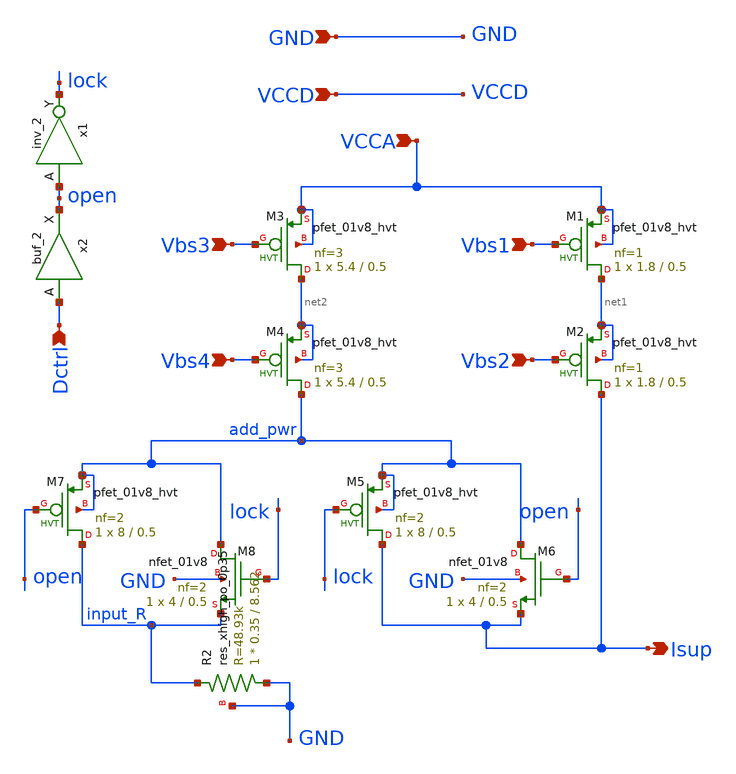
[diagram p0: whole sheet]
** sch_path: xschem/lib_dco/dco_idac.sch
**.subckt dco_idac Vbs3 Vbs4 Vbs1 Vbs2 Isup Dctrl VCCA GND VCCD
*.ipin Vbs3
*.ipin Vbs4
*.ipin Vbs1
*.ipin Vbs2
*.opin Isup
*.ipin Dctrl
*.ipin VCCA
*.ipin GND
*.ipin VCCD
x1 open GND GND VCCD VCCD lock sky130_fd_sc_hd__inv_2
XM1 net1 Vbs1 VCCA VCCA sky130_fd_pr__pfet_01v8_hvt L=0.5 W=1.8 nf=1 ad='int((nf+1)/2) * W/nf * 0.29'
+ as='int((nf+2)/2) * W/nf * 0.29' pd='2*int((nf+1)/2) * (W/nf + 0.29)' ps='2*int((nf+2)/2) * (W/nf + 0.29)'
+ nrd='0.29 / W' nrs='0.29 / W' sa=0 sb=0 sd=0 mult=1 m=1
XM2 Isup Vbs2 net1 net1 sky130_fd_pr__pfet_01v8_hvt L=0.5 W=1.8 nf=1 ad='int((nf+1)/2) * W/nf * 0.29'
+ as='int((nf+2)/2) * W/nf * 0.29' pd='2*int((nf+1)/2) * (W/nf + 0.29)' ps='2*int((nf+2)/2) * (W/nf + 0.29)'
+ nrd='0.29 / W' nrs='0.29 / W' sa=0 sb=0 sd=0 mult=1 m=1
x2 Dctrl GND GND VCCD VCCD open sky130_fd_sc_hd__buf_2
XM3 net2 Vbs3 VCCA VCCA sky130_fd_pr__pfet_01v8_hvt L=0.5 W=5.4 nf=3 ad='int((nf+1)/2) * W/nf * 0.29'
+ as='int((nf+2)/2) * W/nf * 0.29' pd='2*int((nf+1)/2) * (W/nf + 0.29)' ps='2*int((nf+2)/2) * (W/nf + 0.29)'
+ nrd='0.29 / W' nrs='0.29 / W' sa=0 sb=0 sd=0 mult=1 m=1
XM4 add_pwr Vbs4 net2 net2 sky130_fd_pr__pfet_01v8_hvt L=0.5 W=5.4 nf=3 ad='int((nf+1)/2) * W/nf * 0.29'
+ as='int((nf+2)/2) * W/nf * 0.29' pd='2*int((nf+1)/2) * (W/nf + 0.29)' ps='2*int((nf+2)/2) * (W/nf + 0.29)'
+ nrd='0.29 / W' nrs='0.29 / W' sa=0 sb=0 sd=0 mult=1 m=1
XM5 Isup lock add_pwr add_pwr sky130_fd_pr__pfet_01v8_hvt L=0.5 W=8 nf=2 ad='int((nf+1)/2) * W/nf * 0.29'
+ as='int((nf+2)/2) * W/nf * 0.29' pd='2*int((nf+1)/2) * (W/nf + 0.29)' ps='2*int((nf+2)/2) * (W/nf + 0.29)'
+ nrd='0.29 / W' nrs='0.29 / W' sa=0 sb=0 sd=0 mult=1 m=1
XM6 add_pwr open Isup GND sky130_fd_pr__nfet_01v8 L=0.5 W=4 nf=2 ad='int((nf+1)/2) * W/nf * 0.29' as='int((nf+2)/2) * W/nf * 0.29'
+ pd='2*int((nf+1)/2) * (W/nf + 0.29)' ps='2*int((nf+2)/2) * (W/nf + 0.29)' nrd='0.29 / W' nrs='0.29 / W'
+ sa=0 sb=0 sd=0 mult=1 m=1
XM7 input_R open add_pwr add_pwr sky130_fd_pr__pfet_01v8_hvt L=0.5 W=8 nf=2 ad='int((nf+1)/2) * W/nf * 0.29'
+ as='int((nf+2)/2) * W/nf * 0.29' pd='2*int((nf+1)/2) * (W/nf + 0.29)' ps='2*int((nf+2)/2) * (W/nf + 0.29)'
+ nrd='0.29 / W' nrs='0.29 / W' sa=0 sb=0 sd=0 mult=1 m=1
XM8 add_pwr lock input_R GND sky130_fd_pr__nfet_01v8 L=0.5 W=4 nf=2 ad='int((nf+1)/2) * W/nf * 0.29'
+ as='int((nf+2)/2) * W/nf * 0.29' pd='2*int((nf+1)/2) * (W/nf + 0.29)' ps='2*int((nf+2)/2) * (W/nf + 0.29)'
+ nrd='0.29 / W' nrs='0.29 / W' sa=0 sb=0 sd=0 mult=1 m=1
XR2 GND input_R GND sky130_fd_pr__res_xhigh_po_0p35 L=8.562 mult=1 m=1
**.ends
.end
